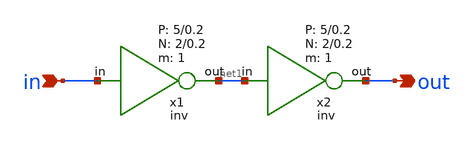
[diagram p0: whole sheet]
** sch_path: design/schematic/buffer.sch
**.subckt buffer in out
*.ipin in
*.opin out
x1 in net1 VDD GND 1 2 0.2 5 0.2 inv
x2 net1 out VDD GND 1 2 0.2 5 0.2 inv
**.ends

* expanding   symbol:  inv.sym # of pins=2
** sym_path: design/schematic/inv.sym
** sch_path: design/schematic/inv.sch
.subckt inv in out VDD VSS N W_N L_N W_P L_P    N=1 W_N=2 L_N=0.2 W_P=5 L_P=0.2
*.ipin in
*.opin out
XM2 out in VSS VSS sky130_fd_pr__nfet_01v8 L=L_N W=W_N nf=1 ad='int((nf+1)/2) * W/nf * 0.29' as='int((nf+2)/2) * W/nf * 0.29'
+ pd='2*int((nf+1)/2) * (W/nf + 0.29)' ps='2*int((nf+2)/2) * (W/nf + 0.29)' nrd='0.29 / W' nrs='0.29 / W'
+ sa=0 sb=0 sd=0 mult=N m=N
XM1 out in VDD VDD sky130_fd_pr__pfet_01v8 L=L_P W=W_P nf=1 ad='int((nf+1)/2) * W/nf * 0.29' as='int((nf+2)/2) * W/nf * 0.29'
+ pd='2*int((nf+1)/2) * (W/nf + 0.29)' ps='2*int((nf+2)/2) * (W/nf + 0.29)' nrd='0.29 / W' nrs='0.29 / W'
+ sa=0 sb=0 sd=0 mult=N m=N
.ends

.end
